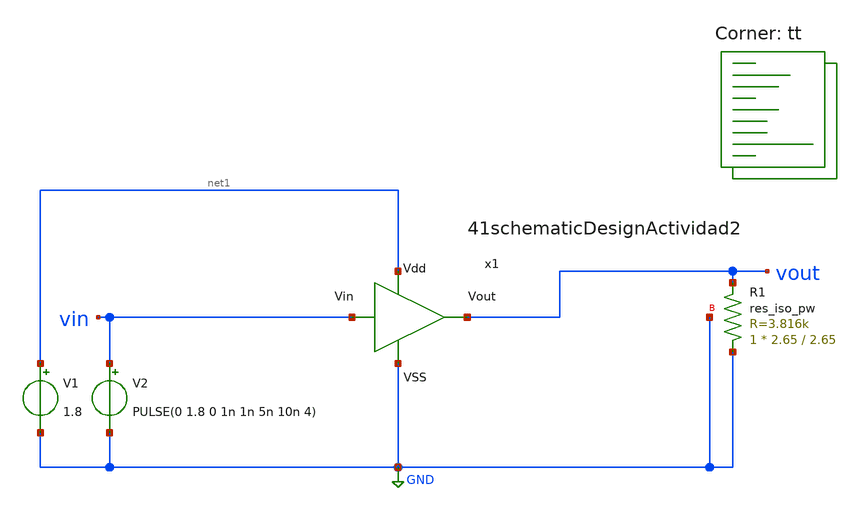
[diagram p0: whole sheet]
** sch_path: trabajosPracticos/Informes - Rao V Parfait M Gatica M - 3R1 - Dispositivos electrónicos/TP6 - CMOS - Rao Parfait Gatica - 3R1/archivosXschem/42simulation.sch

.include /home/marcosgatica/pdk/sky130B/libs.ref/sky130_fd_sc_hd/spice/sky130_fd_sc_hd.spice

**.subckt 42simulation
V1 net1 GND 1.8
V2 vin GND PULSE(0 1.8 0 1n 1n 5n 10n 4)
XR1 GND vout GND sky130_fd_pr__res_iso_pw W=2.65 L=2.65 m=1
x1 net1 vin vout GND 41schematicDesignActividad2
**** begin user architecture code
.lib $::SKYWATER_MODELS/sky130.lib.spice tt


.control
	run
	tran 0.5n 40n
	write std_not4_tb.raw
.endc
.save all


**** end user architecture code
**.ends
.GLOBAL GND
.end
